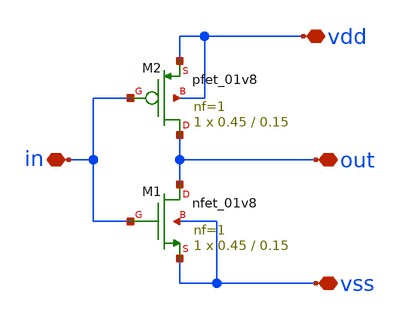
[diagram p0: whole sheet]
** sch_path: Custom_std_cells/inverter.sch
**.subckt inverter vdd vss out in
*.iopin vdd
*.iopin vss
*.iopin out
*.iopin in
XM1 out in vss vss sky130_fd_pr__nfet_01v8 L=0.15 W=0.45 nf=1 ad='int((1 + 1)/2) * 0.45 / 1 * 0.29' as='int((1 + 2)/2) * 0.45 / 1 * 0.29'
+ pd='2*int((1 + 1)/2) * (0.45 / 1 + 0.29)' ps='2*int((1 + 2)/2) * (0.45 / 1 + 0.29)' nrd='0.29 / 0.45 '
+ nrs='0.29 / 0.45 ' sa=0 sb=0 sd=0 mult=1 m=1
XM2 out in vdd vdd sky130_fd_pr__pfet_01v8 L=0.15 W=0.45 nf=1 ad='int((1 + 1)/2) * 0.45 / 1 * 0.29' as='int((1 + 2)/2) * 0.45 / 1 * 0.29'
+ pd='2*int((1 + 1)/2) * (0.45 / 1 + 0.29)' ps='2*int((1 + 2)/2) * (0.45 / 1 + 0.29)' nrd='0.29 / 0.45 '
+ nrs='0.29 / 0.45 ' sa=0 sb=0 sd=0 mult=1 m=1
**.ends
.end
